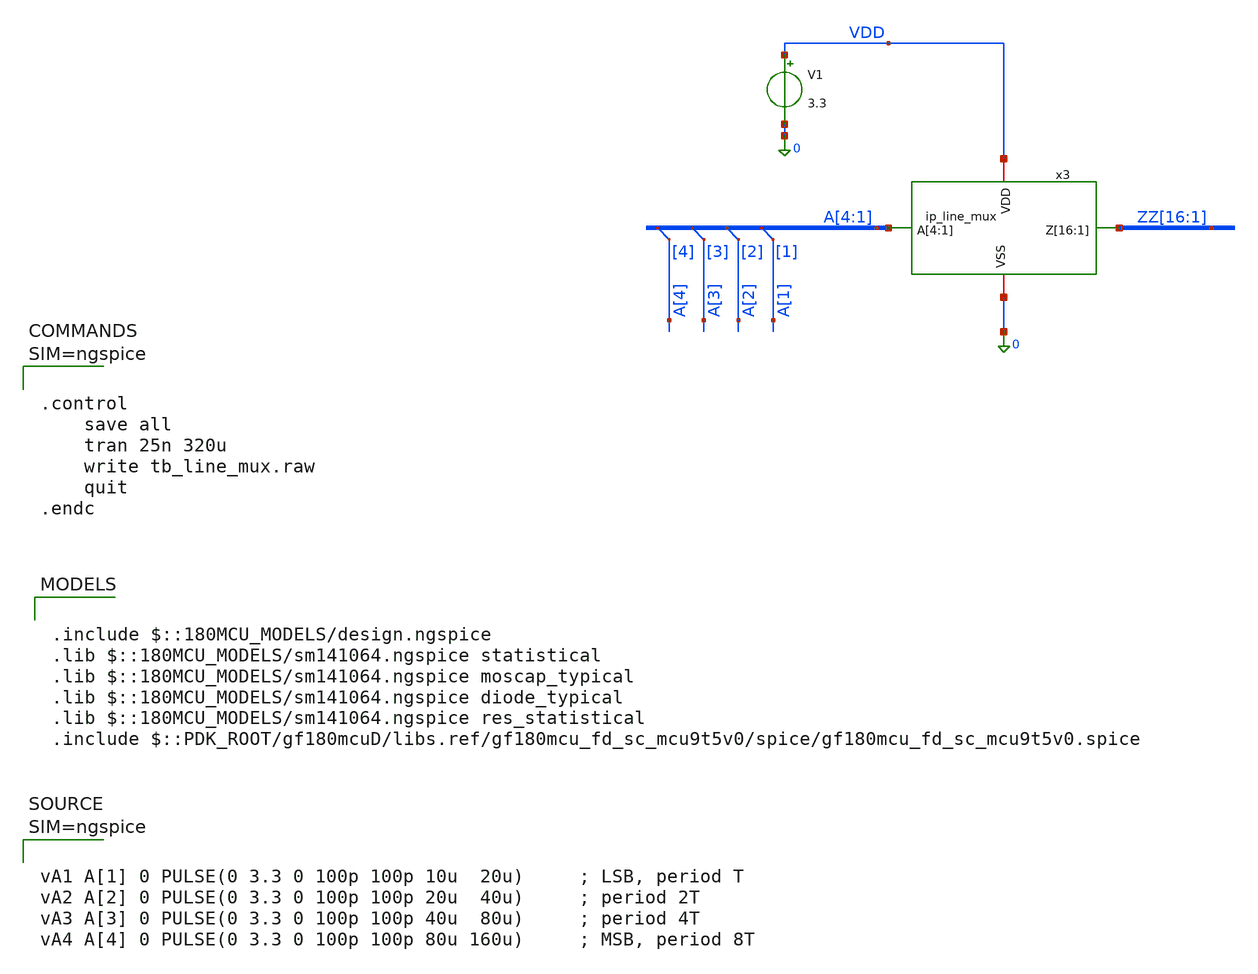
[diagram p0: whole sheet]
** sch_path: xschem/tb_line_mux.sch
**.subckt tb_line_mux
V1 VDD 0 3.3
x3 VDD 0 A[4] A[3] A[2] A[1] ZZ[16] ZZ[15] ZZ[14] ZZ[13] ZZ[12] ZZ[11] ZZ[10] ZZ[9] ZZ[8] ZZ[7]
+ ZZ[6] ZZ[5] ZZ[4] ZZ[3] ZZ[2] ZZ[1] ip_line_mux
* tap: A[4:1] --> A[4]
* tap: A[4:1] --> A[3]
* tap: A[4:1] --> A[2]
* tap: A[4:1] --> A[1]
**** begin user architecture code

.include $::180MCU_MODELS/design.ngspice
.lib $::180MCU_MODELS/sm141064.ngspice statistical
.lib $::180MCU_MODELS/sm141064.ngspice moscap_typical
.lib $::180MCU_MODELS/sm141064.ngspice diode_typical
.lib $::180MCU_MODELS/sm141064.ngspice res_statistical
.include $::PDK_ROOT/gf180mcuD/libs.ref/gf180mcu_fd_sc_mcu9t5v0/spice/gf180mcu_fd_sc_mcu9t5v0.spice




.control
	save all
	tran 25n 320u
	write tb_line_mux.raw
	quit
.endc






vA1 A[1] 0 PULSE(0 3.3 0 100p 100p 10u  20u)     ; LSB, period T
vA2 A[2] 0 PULSE(0 3.3 0 100p 100p 20u  40u)     ; period 2T
vA3 A[3] 0 PULSE(0 3.3 0 100p 100p 40u  80u)     ; period 4T
vA4 A[4] 0 PULSE(0 3.3 0 100p 100p 80u 160u)     ; MSB, period 8T



**** end user architecture code
**.ends

* expanding   symbol:  ip_line_mux.sym # of pins=4
** sym_path: xschem/ip_line_mux.sym
** sch_path: xschem/ip_line_mux.sch
.subckt ip_line_mux VDD VSS A[4] A[3] A[2] A[1] Z[16] Z[15] Z[14] Z[13] Z[12] Z[11] Z[10] Z[9] Z[8]
+ Z[7] Z[6] Z[5] Z[4] Z[3] Z[2] Z[1]
*.ipin A[4],A[3],A[2],A[1]
*.iopin VDD
*.iopin VSS
*.opin Z[16],Z[15],Z[14],Z[13],Z[12],Z[11],Z[10],Z[9],Z[8],Z[7],Z[6],Z[5],Z[4],Z[3],Z[2],Z[1]
x1 A[2] A2B VDD VDD VSS VSS gf180mcu_fd_sc_mcu9t5v0__inv_1
x2 A4B A3B A2B A1B Z[1] VDD VDD VSS VSS gf180mcu_fd_sc_mcu9t5v0__and4_1
x3 A[1] A1B VDD VDD VSS VSS gf180mcu_fd_sc_mcu9t5v0__inv_1
x4 A[3] A3B VDD VDD VSS VSS gf180mcu_fd_sc_mcu9t5v0__inv_1
x5 A[4] A4B VDD VDD VSS VSS gf180mcu_fd_sc_mcu9t5v0__inv_1
* tap: A[4:1] --> A[4]
* tap: A[4:1] --> A[3]
* tap: A[4:1] --> A[2]
* tap: A[4:1] --> A[1]
* tap: Z[16:1] --> Z[1]
* tap: Z[16:1] --> Z[2]
* tap: Z[16:1] --> Z[3]
* tap: Z[16:1] --> Z[4]
* tap: Z[16:1] --> Z[5]
* tap: Z[16:1] --> Z[6]
* tap: Z[16:1] --> Z[7]
* tap: Z[16:1] --> Z[8]
* tap: Z[16:1] --> Z[9]
* tap: Z[16:1] --> Z[10]
* tap: Z[16:1] --> Z[11]
* tap: Z[16:1] --> Z[12]
* tap: Z[16:1] --> Z[13]
* tap: Z[16:1] --> Z[14]
* tap: Z[16:1] --> Z[15]
* tap: Z[16:1] --> Z[16]
x6 A4B A3B A2B A[1] Z[2] VDD VDD VSS VSS gf180mcu_fd_sc_mcu9t5v0__and4_1
x7 A4B A3B A[2] A1B Z[3] VDD VDD VSS VSS gf180mcu_fd_sc_mcu9t5v0__and4_1
x8 A4B A3B A[2] A[1] Z[4] VDD VDD VSS VSS gf180mcu_fd_sc_mcu9t5v0__and4_1
x9 A4B A[3] A2B A1B Z[5] VDD VDD VSS VSS gf180mcu_fd_sc_mcu9t5v0__and4_1
x10 A4B A[3] A2B A[1] Z[6] VDD VDD VSS VSS gf180mcu_fd_sc_mcu9t5v0__and4_1
x11 A4B A[3] A[2] A1B Z[7] VDD VDD VSS VSS gf180mcu_fd_sc_mcu9t5v0__and4_1
x12 A4B A[3] A[2] A[1] Z[8] VDD VDD VSS VSS gf180mcu_fd_sc_mcu9t5v0__and4_1
x13 A[4] A3B A2B A1B Z[9] VDD VDD VSS VSS gf180mcu_fd_sc_mcu9t5v0__and4_1
x14 A[4] A3B A2B A[1] Z[10] VDD VDD VSS VSS gf180mcu_fd_sc_mcu9t5v0__and4_1
x15 A[4] A3B A[2] A1B Z[11] VDD VDD VSS VSS gf180mcu_fd_sc_mcu9t5v0__and4_1
x16 A[4] A3B A[2] A[1] Z[12] VDD VDD VSS VSS gf180mcu_fd_sc_mcu9t5v0__and4_1
x17 A[4] A[3] A2B A1B Z[13] VDD VDD VSS VSS gf180mcu_fd_sc_mcu9t5v0__and4_1
x18 A[4] A[3] A2B A[1] Z[14] VDD VDD VSS VSS gf180mcu_fd_sc_mcu9t5v0__and4_1
x19 A[4] A[3] A[2] A1B Z[15] VDD VDD VSS VSS gf180mcu_fd_sc_mcu9t5v0__and4_1
x20 A[4] A[3] A[2] A[1] Z[16] VDD VDD VSS VSS gf180mcu_fd_sc_mcu9t5v0__and4_1
.ends

.end
